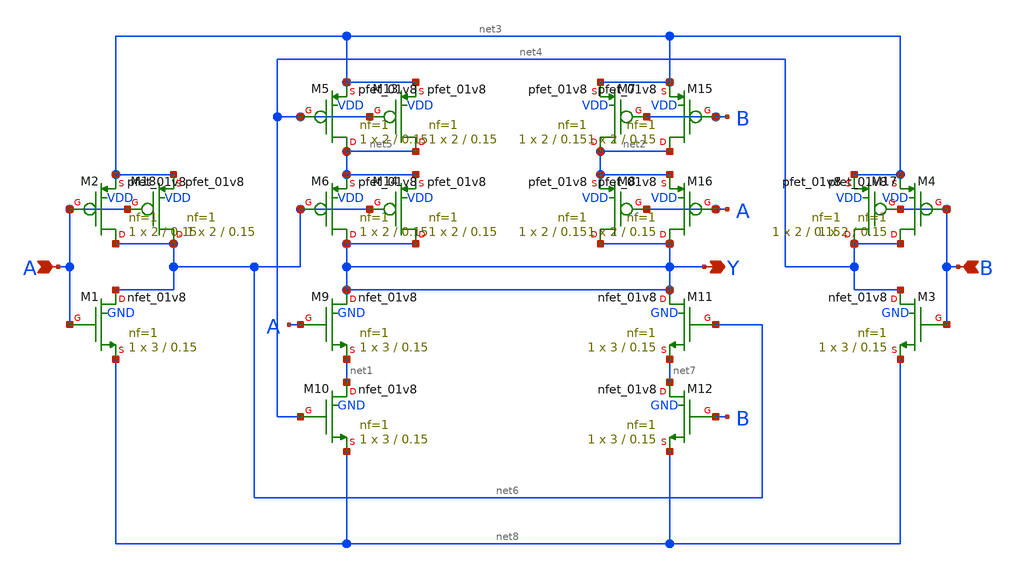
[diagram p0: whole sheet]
** sch_path: lib/xschem/XNOR2X1.sch
**.subckt XNOR2X1 A Y B
*.ipin A
*.opin Y
*.ipin B
XM1 net6 A net8 GND sky130_fd_pr__nfet_01v8 L=0.15 W=3 nf=1 ad='int((nf+1)/2) * W/nf * 0.29' as='int((nf+2)/2) * W/nf * 0.29'
+ pd='2*int((nf+1)/2) * (W/nf + 0.29)' ps='2*int((nf+2)/2) * (W/nf + 0.29)' nrd='0.29 / W' nrs='0.29 / W'
+ sa=0 sb=0 sd=0 mult=1 m=1
XM2 net6 A net3 VDD sky130_fd_pr__pfet_01v8 L=0.15 W=2 nf=1 ad='int((nf+1)/2) * W/nf * 0.29' as='int((nf+2)/2) * W/nf * 0.29'
+ pd='2*int((nf+1)/2) * (W/nf + 0.29)' ps='2*int((nf+2)/2) * (W/nf + 0.29)' nrd='0.29 / W' nrs='0.29 / W'
+ sa=0 sb=0 sd=0 mult=1 m=1
XM3 net4 B net8 GND sky130_fd_pr__nfet_01v8 L=0.15 W=3 nf=1 ad='int((nf+1)/2) * W/nf * 0.29' as='int((nf+2)/2) * W/nf * 0.29'
+ pd='2*int((nf+1)/2) * (W/nf + 0.29)' ps='2*int((nf+2)/2) * (W/nf + 0.29)' nrd='0.29 / W' nrs='0.29 / W'
+ sa=0 sb=0 sd=0 mult=1 m=1
XM4 net4 B net3 VDD sky130_fd_pr__pfet_01v8 L=0.15 W=2 nf=1 ad='int((nf+1)/2) * W/nf * 0.29' as='int((nf+2)/2) * W/nf * 0.29'
+ pd='2*int((nf+1)/2) * (W/nf + 0.29)' ps='2*int((nf+2)/2) * (W/nf + 0.29)' nrd='0.29 / W' nrs='0.29 / W'
+ sa=0 sb=0 sd=0 mult=1 m=1
XM5 net5 net4 net3 VDD sky130_fd_pr__pfet_01v8 L=0.15 W=2 nf=1 ad='int((nf+1)/2) * W/nf * 0.29' as='int((nf+2)/2) * W/nf * 0.29'
+ pd='2*int((nf+1)/2) * (W/nf + 0.29)' ps='2*int((nf+2)/2) * (W/nf + 0.29)' nrd='0.29 / W' nrs='0.29 / W'
+ sa=0 sb=0 sd=0 mult=1 m=1
XM6 Y net6 net5 VDD sky130_fd_pr__pfet_01v8 L=0.15 W=2 nf=1 ad='int((nf+1)/2) * W/nf * 0.29' as='int((nf+2)/2) * W/nf * 0.29'
+ pd='2*int((nf+1)/2) * (W/nf + 0.29)' ps='2*int((nf+2)/2) * (W/nf + 0.29)' nrd='0.29 / W' nrs='0.29 / W'
+ sa=0 sb=0 sd=0 mult=1 m=1
XM7 net2 B net3 VDD sky130_fd_pr__pfet_01v8 L=0.15 W=2 nf=1 ad='int((nf+1)/2) * W/nf * 0.29' as='int((nf+2)/2) * W/nf * 0.29'
+ pd='2*int((nf+1)/2) * (W/nf + 0.29)' ps='2*int((nf+2)/2) * (W/nf + 0.29)' nrd='0.29 / W' nrs='0.29 / W'
+ sa=0 sb=0 sd=0 mult=1 m=1
XM8 Y A net2 VDD sky130_fd_pr__pfet_01v8 L=0.15 W=2 nf=1 ad='int((nf+1)/2) * W/nf * 0.29' as='int((nf+2)/2) * W/nf * 0.29'
+ pd='2*int((nf+1)/2) * (W/nf + 0.29)' ps='2*int((nf+2)/2) * (W/nf + 0.29)' nrd='0.29 / W' nrs='0.29 / W'
+ sa=0 sb=0 sd=0 mult=1 m=1
XM9 Y A net1 GND sky130_fd_pr__nfet_01v8 L=0.15 W=3 nf=1 ad='int((nf+1)/2) * W/nf * 0.29' as='int((nf+2)/2) * W/nf * 0.29'
+ pd='2*int((nf+1)/2) * (W/nf + 0.29)' ps='2*int((nf+2)/2) * (W/nf + 0.29)' nrd='0.29 / W' nrs='0.29 / W'
+ sa=0 sb=0 sd=0 mult=1 m=1
XM10 net1 net4 net8 GND sky130_fd_pr__nfet_01v8 L=0.15 W=3 nf=1 ad='int((nf+1)/2) * W/nf * 0.29' as='int((nf+2)/2) * W/nf * 0.29'
+ pd='2*int((nf+1)/2) * (W/nf + 0.29)' ps='2*int((nf+2)/2) * (W/nf + 0.29)' nrd='0.29 / W' nrs='0.29 / W'
+ sa=0 sb=0 sd=0 mult=1 m=1
XM11 Y net6 net7 GND sky130_fd_pr__nfet_01v8 L=0.15 W=3 nf=1 ad='int((nf+1)/2) * W/nf * 0.29' as='int((nf+2)/2) * W/nf * 0.29'
+ pd='2*int((nf+1)/2) * (W/nf + 0.29)' ps='2*int((nf+2)/2) * (W/nf + 0.29)' nrd='0.29 / W' nrs='0.29 / W'
+ sa=0 sb=0 sd=0 mult=1 m=1
XM12 net7 B net8 GND sky130_fd_pr__nfet_01v8 L=0.15 W=3 nf=1 ad='int((nf+1)/2) * W/nf * 0.29' as='int((nf+2)/2) * W/nf * 0.29'
+ pd='2*int((nf+1)/2) * (W/nf + 0.29)' ps='2*int((nf+2)/2) * (W/nf + 0.29)' nrd='0.29 / W' nrs='0.29 / W'
+ sa=0 sb=0 sd=0 mult=1 m=1
XM13 net5 net4 net3 VDD sky130_fd_pr__pfet_01v8 L=0.15 W=2 nf=1 ad='int((nf+1)/2) * W/nf * 0.29' as='int((nf+2)/2) * W/nf * 0.29'
+ pd='2*int((nf+1)/2) * (W/nf + 0.29)' ps='2*int((nf+2)/2) * (W/nf + 0.29)' nrd='0.29 / W' nrs='0.29 / W'
+ sa=0 sb=0 sd=0 mult=1 m=1
XM14 Y net6 net5 VDD sky130_fd_pr__pfet_01v8 L=0.15 W=2 nf=1 ad='int((nf+1)/2) * W/nf * 0.29' as='int((nf+2)/2) * W/nf * 0.29'
+ pd='2*int((nf+1)/2) * (W/nf + 0.29)' ps='2*int((nf+2)/2) * (W/nf + 0.29)' nrd='0.29 / W' nrs='0.29 / W'
+ sa=0 sb=0 sd=0 mult=1 m=1
XM15 net2 B net3 VDD sky130_fd_pr__pfet_01v8 L=0.15 W=2 nf=1 ad='int((nf+1)/2) * W/nf * 0.29' as='int((nf+2)/2) * W/nf * 0.29'
+ pd='2*int((nf+1)/2) * (W/nf + 0.29)' ps='2*int((nf+2)/2) * (W/nf + 0.29)' nrd='0.29 / W' nrs='0.29 / W'
+ sa=0 sb=0 sd=0 mult=1 m=1
XM16 Y A net2 VDD sky130_fd_pr__pfet_01v8 L=0.15 W=2 nf=1 ad='int((nf+1)/2) * W/nf * 0.29' as='int((nf+2)/2) * W/nf * 0.29'
+ pd='2*int((nf+1)/2) * (W/nf + 0.29)' ps='2*int((nf+2)/2) * (W/nf + 0.29)' nrd='0.29 / W' nrs='0.29 / W'
+ sa=0 sb=0 sd=0 mult=1 m=1
XM17 net4 B net3 VDD sky130_fd_pr__pfet_01v8 L=0.15 W=2 nf=1 ad='int((nf+1)/2) * W/nf * 0.29' as='int((nf+2)/2) * W/nf * 0.29'
+ pd='2*int((nf+1)/2) * (W/nf + 0.29)' ps='2*int((nf+2)/2) * (W/nf + 0.29)' nrd='0.29 / W' nrs='0.29 / W'
+ sa=0 sb=0 sd=0 mult=1 m=1
XM18 net6 A net3 VDD sky130_fd_pr__pfet_01v8 L=0.15 W=2 nf=1 ad='int((nf+1)/2) * W/nf * 0.29' as='int((nf+2)/2) * W/nf * 0.29'
+ pd='2*int((nf+1)/2) * (W/nf + 0.29)' ps='2*int((nf+2)/2) * (W/nf + 0.29)' nrd='0.29 / W' nrs='0.29 / W'
+ sa=0 sb=0 sd=0 mult=1 m=1
**.ends
.end
